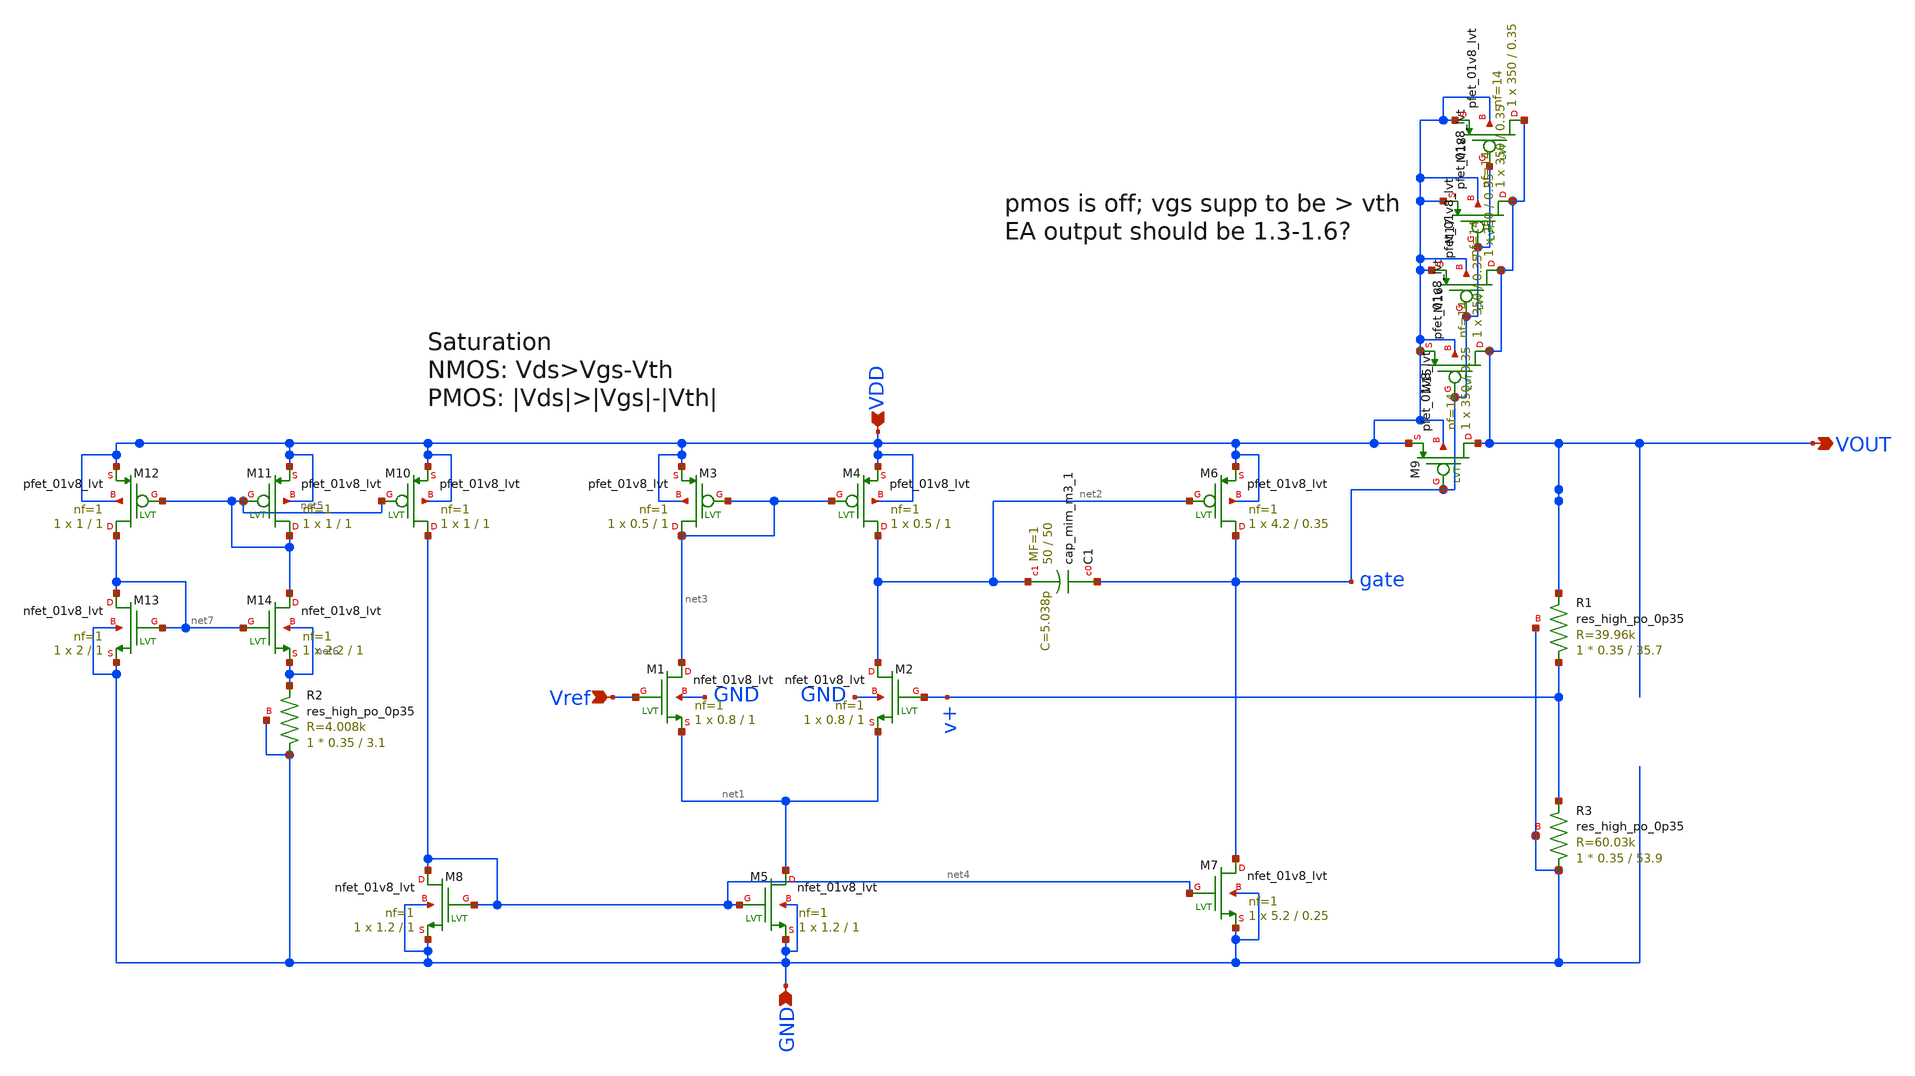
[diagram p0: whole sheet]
** sch_path: xschem/UREx-LDO-v4.sch
**.subckt UREx-LDO-v4 VDD VOUT GND Vref
*.ipin VDD
*.opin VOUT
*.ipin GND
*.ipin Vref
XM1 net3 Vref net1 GND sky130_fd_pr__nfet_01v8_lvt L=1 W=0.8 nf=1 ad='int((1 + 1)/2) * 0.8 / 1 * 0.29'
+ as='int((1 + 2)/2) * 0.8 / 1 * 0.29' pd='2*int((1 + 1)/2) * (0.8 / 1 + 0.29)' ps='2*int((1 + 2)/2) * (0.8 / 1 + 0.29)'
+ nrd='0.29 / 0.8 ' nrs='0.29 / 0.8 ' sa=0 sb=0 sd=0 mult=1 m=1
XM2 net2 v+ net1 GND sky130_fd_pr__nfet_01v8_lvt L=1 W=0.8 nf=1 ad='int((1 + 1)/2) * 0.8 / 1 * 0.29'
+ as='int((1 + 2)/2) * 0.8 / 1 * 0.29' pd='2*int((1 + 1)/2) * (0.8 / 1 + 0.29)' ps='2*int((1 + 2)/2) * (0.8 / 1 + 0.29)'
+ nrd='0.29 / 0.8 ' nrs='0.29 / 0.8 ' sa=0 sb=0 sd=0 mult=1 m=1
XM4 net2 net3 VDD VDD sky130_fd_pr__pfet_01v8_lvt L=1 W=0.5 nf=1 ad='int((1 + 1)/2) * 0.5 / 1 * 0.29'
+ as='int((1 + 2)/2) * 0.5 / 1 * 0.29' pd='2*int((1 + 1)/2) * (0.5 / 1 + 0.29)' ps='2*int((1 + 2)/2) * (0.5 / 1 + 0.29)'
+ nrd='0.29 / 0.5 ' nrs='0.29 / 0.5 ' sa=0 sb=0 sd=0 mult=1 m=1
XM3 net3 net3 VDD VDD sky130_fd_pr__pfet_01v8_lvt L=1 W=0.5 nf=1 ad='int((1 + 1)/2) * 0.5 / 1 * 0.29'
+ as='int((1 + 2)/2) * 0.5 / 1 * 0.29' pd='2*int((1 + 1)/2) * (0.5 / 1 + 0.29)' ps='2*int((1 + 2)/2) * (0.5 / 1 + 0.29)'
+ nrd='0.29 / 0.5 ' nrs='0.29 / 0.5 ' sa=0 sb=0 sd=0 mult=1 m=1
XM6 gate net2 VDD VDD sky130_fd_pr__pfet_01v8_lvt L=0.35 W=4.2 nf=1 ad='int((1 + 1)/2) * 4.2 / 1 * 0.29'
+ as='int((1 + 2)/2) * 4.2 / 1 * 0.29' pd='2*int((1 + 1)/2) * (4.2 / 1 + 0.29)' ps='2*int((1 + 2)/2) * (4.2 / 1 + 0.29)'
+ nrd='0.29 / 4.2 ' nrs='0.29 / 4.2 ' sa=0 sb=0 sd=0 mult=1 m=1
XM7 gate net4 GND GND sky130_fd_pr__nfet_01v8_lvt L=0.25 W=5.2 nf=1 ad='int((1 + 1)/2) * 5.2 / 1 * 0.29'
+ as='int((1 + 2)/2) * 5.2 / 1 * 0.29' pd='2*int((1 + 1)/2) * (5.2 / 1 + 0.29)' ps='2*int((1 + 2)/2) * (5.2 / 1 + 0.29)'
+ nrd='0.29 / 5.2 ' nrs='0.29 / 5.2 ' sa=0 sb=0 sd=0 mult=1 m=1
XM9 VOUT gate VDD VDD sky130_fd_pr__pfet_01v8_lvt L=0.35 W=350 nf=14 ad='int((14 + 1)/2) * 350 / 14 * 0.29'
+ as='int((14 + 2)/2) * 350 / 14 * 0.29' pd='2*int((14 + 1)/2) * (350 / 14 + 0.29)' ps='2*int((14 + 2)/2) * (350 / 14 + 0.29)'
+ nrd='0.29 / 350 ' nrs='0.29 / 350 ' sa=0 sb=0 sd=0 mult=1 m=1
XM10 net4 net5 VDD VDD sky130_fd_pr__pfet_01v8_lvt L=1 W=1 nf=1 ad='int((1 + 1)/2) * 1 / 1 * 0.29' as='int((1 + 2)/2) * 1 / 1 * 0.29'
+ pd='2*int((1 + 1)/2) * (1 / 1 + 0.29)' ps='2*int((1 + 2)/2) * (1 / 1 + 0.29)' nrd='0.29 / 1 ' nrs='0.29 / 1 '
+ sa=0 sb=0 sd=0 mult=1 m=1
XM11 net5 net5 VDD VDD sky130_fd_pr__pfet_01v8_lvt L=1 W=1 nf=1 ad='int((1 + 1)/2) * 1 / 1 * 0.29' as='int((1 + 2)/2) * 1 / 1 * 0.29'
+ pd='2*int((1 + 1)/2) * (1 / 1 + 0.29)' ps='2*int((1 + 2)/2) * (1 / 1 + 0.29)' nrd='0.29 / 1 ' nrs='0.29 / 1 '
+ sa=0 sb=0 sd=0 mult=1 m=1
XM12 net7 net5 VDD VDD sky130_fd_pr__pfet_01v8_lvt L=1 W=1 nf=1 ad='int((1 + 1)/2) * 1 / 1 * 0.29' as='int((1 + 2)/2) * 1 / 1 * 0.29'
+ pd='2*int((1 + 1)/2) * (1 / 1 + 0.29)' ps='2*int((1 + 2)/2) * (1 / 1 + 0.29)' nrd='0.29 / 1 ' nrs='0.29 / 1 '
+ sa=0 sb=0 sd=0 mult=1 m=1
XM13 net7 net7 GND GND sky130_fd_pr__nfet_01v8_lvt L=1 W=2 nf=1 ad='int((1 + 1)/2) * 2 / 1 * 0.29' as='int((1 + 2)/2) * 2 / 1 * 0.29'
+ pd='2*int((1 + 1)/2) * (2 / 1 + 0.29)' ps='2*int((1 + 2)/2) * (2 / 1 + 0.29)' nrd='0.29 / 2 ' nrs='0.29 / 2 '
+ sa=0 sb=0 sd=0 mult=1 m=1
XM14 net5 net7 net6 net6 sky130_fd_pr__nfet_01v8_lvt L=1 W=2.2 nf=1 ad='int((1 + 1)/2) * 2.2 / 1 * 0.29'
+ as='int((1 + 2)/2) * 2.2 / 1 * 0.29' pd='2*int((1 + 1)/2) * (2.2 / 1 + 0.29)' ps='2*int((1 + 2)/2) * (2.2 / 1 + 0.29)'
+ nrd='0.29 / 2.2 ' nrs='0.29 / 2.2 ' sa=0 sb=0 sd=0 mult=1 m=1
XR1 v+ VOUT GND sky130_fd_pr__res_high_po_0p35 L=35.7 mult=1 m=1
XR3 GND v+ GND sky130_fd_pr__res_high_po_0p35 L=53.9 mult=1 m=1
XR2 GND net6 GND sky130_fd_pr__res_high_po_0p35 L=3.1 mult=1 m=1
XC1 gate net2 sky130_fd_pr__cap_mim_m3_1 W=50 L=50 MF=1 m=1
XM5 net1 net4 GND GND sky130_fd_pr__nfet_01v8_lvt L=1 W=1.2 nf=1 ad='int((1 + 1)/2) * 1.2 / 1 * 0.29'
+ as='int((1 + 2)/2) * 1.2 / 1 * 0.29' pd='2*int((1 + 1)/2) * (1.2 / 1 + 0.29)' ps='2*int((1 + 2)/2) * (1.2 / 1 + 0.29)'
+ nrd='0.29 / 1.2 ' nrs='0.29 / 1.2 ' sa=0 sb=0 sd=0 mult=1 m=1
XM8 net4 net4 GND GND sky130_fd_pr__nfet_01v8_lvt L=1 W=1.2 nf=1 ad='int((1 + 1)/2) * 1.2 / 1 * 0.29'
+ as='int((1 + 2)/2) * 1.2 / 1 * 0.29' pd='2*int((1 + 1)/2) * (1.2 / 1 + 0.29)' ps='2*int((1 + 2)/2) * (1.2 / 1 + 0.29)'
+ nrd='0.29 / 1.2 ' nrs='0.29 / 1.2 ' sa=0 sb=0 sd=0 mult=1 m=1
XM15 VOUT gate VDD VDD sky130_fd_pr__pfet_01v8_lvt L=0.35 W=350 nf=14 ad='int((14 + 1)/2) * 350 / 14 * 0.29'
+ as='int((14 + 2)/2) * 350 / 14 * 0.29' pd='2*int((14 + 1)/2) * (350 / 14 + 0.29)' ps='2*int((14 + 2)/2) * (350 / 14 + 0.29)'
+ nrd='0.29 / 350 ' nrs='0.29 / 350 ' sa=0 sb=0 sd=0 mult=1 m=1
XM16 VOUT gate VDD VDD sky130_fd_pr__pfet_01v8_lvt L=0.35 W=350 nf=14 ad='int((14 + 1)/2) * 350 / 14 * 0.29'
+ as='int((14 + 2)/2) * 350 / 14 * 0.29' pd='2*int((14 + 1)/2) * (350 / 14 + 0.29)' ps='2*int((14 + 2)/2) * (350 / 14 + 0.29)'
+ nrd='0.29 / 350 ' nrs='0.29 / 350 ' sa=0 sb=0 sd=0 mult=1 m=1
XM17 VOUT gate VDD VDD sky130_fd_pr__pfet_01v8_lvt L=0.35 W=350 nf=14 ad='int((14 + 1)/2) * 350 / 14 * 0.29'
+ as='int((14 + 2)/2) * 350 / 14 * 0.29' pd='2*int((14 + 1)/2) * (350 / 14 + 0.29)' ps='2*int((14 + 2)/2) * (350 / 14 + 0.29)'
+ nrd='0.29 / 350 ' nrs='0.29 / 350 ' sa=0 sb=0 sd=0 mult=1 m=1
XM18 VOUT gate VDD VDD sky130_fd_pr__pfet_01v8_lvt L=0.35 W=350 nf=14 ad='int((14 + 1)/2) * 350 / 14 * 0.29'
+ as='int((14 + 2)/2) * 350 / 14 * 0.29' pd='2*int((14 + 1)/2) * (350 / 14 + 0.29)' ps='2*int((14 + 2)/2) * (350 / 14 + 0.29)'
+ nrd='0.29 / 350 ' nrs='0.29 / 350 ' sa=0 sb=0 sd=0 mult=1 m=1
**.ends
.end
